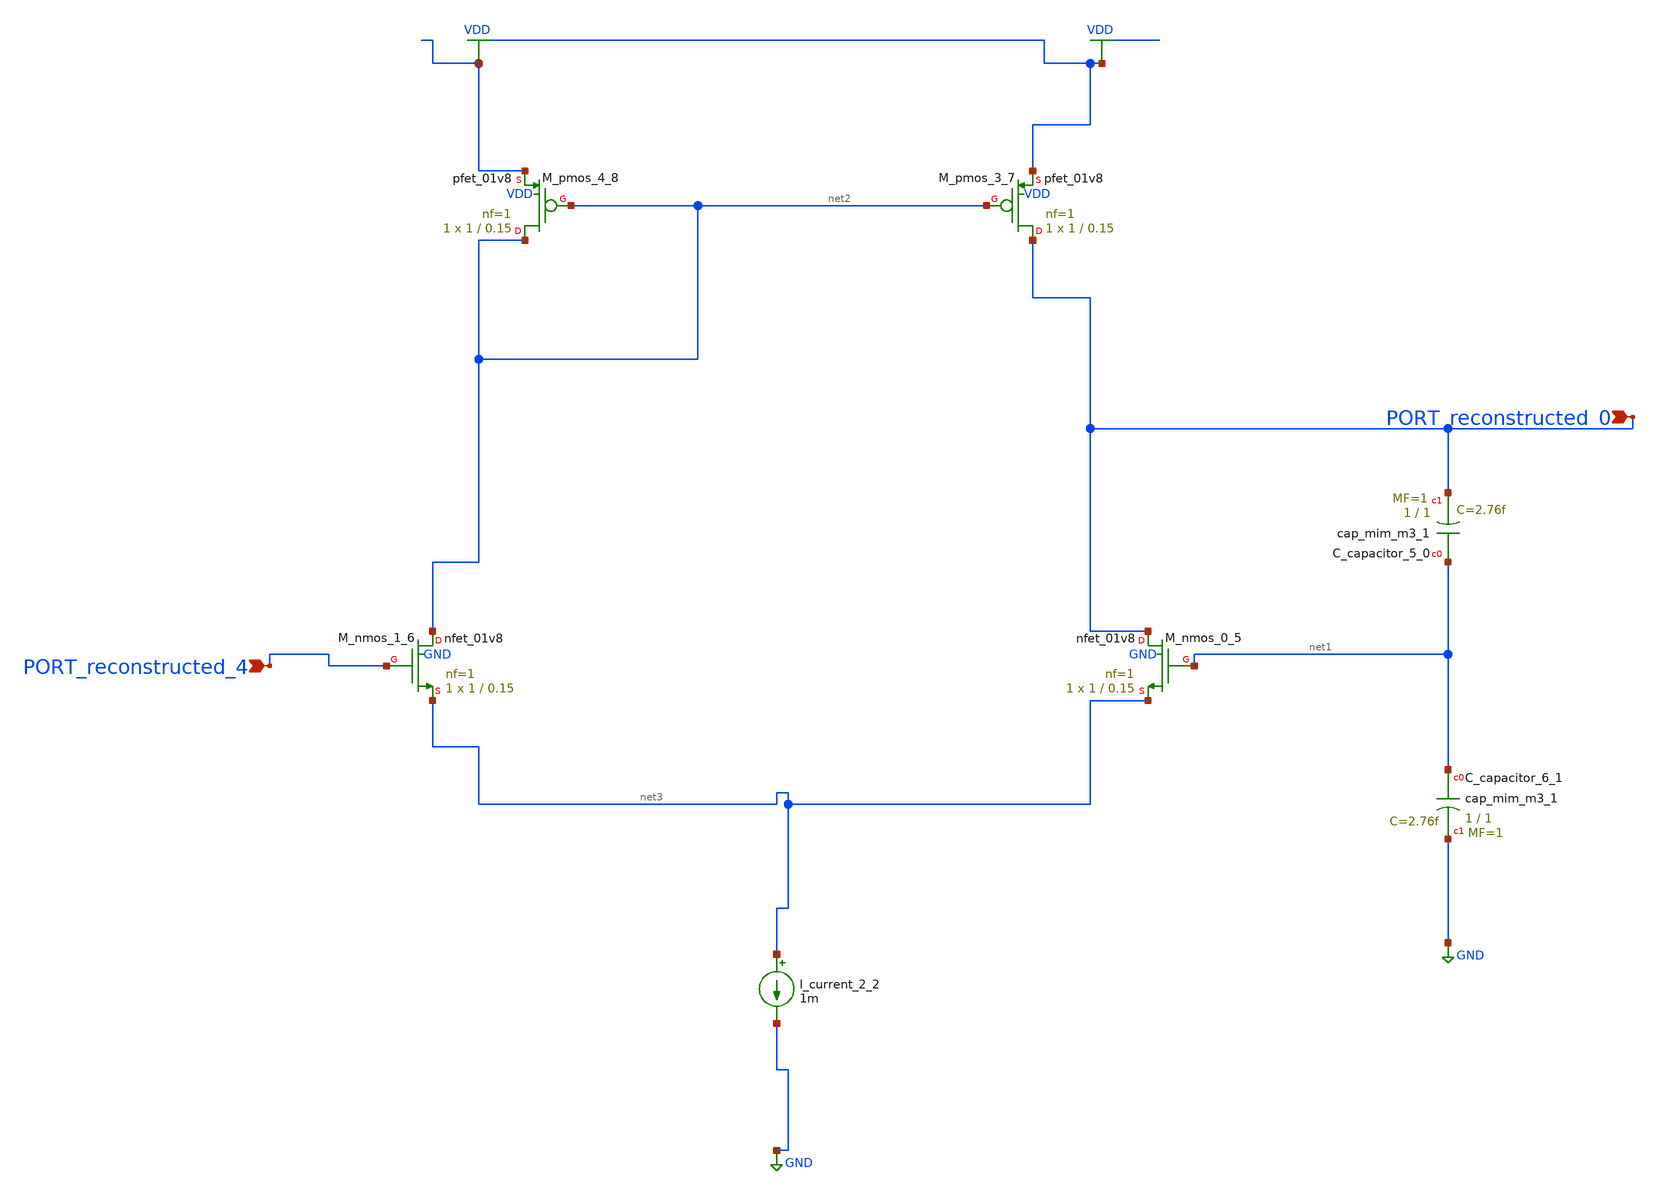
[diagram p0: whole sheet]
** sch_path: schematics/AMSNet/707.sch
**.subckt 707 PORT_reconstructed_0 PORT_reconstructed_4
*.ipin PORT_reconstructed_0
*.ipin PORT_reconstructed_4
XC_capacitor_5_0 net1 PORT_reconstructed_0 sky130_fd_pr__cap_mim_m3_1 W=1 L=1 MF=1 m=1
XC_capacitor_6_1 net1 GND sky130_fd_pr__cap_mim_m3_1 W=1 L=1 MF=1 m=1
I_current_2_2 net3 GND 1m
XM_nmos_0_5 PORT_reconstructed_0 net1 net3 GND sky130_fd_pr__nfet_01v8 L=0.15 W=1 nf=1 ad='int((1 + 1)/2) * 1 / 1 * 0.29'
+ as='int((1 + 2)/2) * 1 / 1 * 0.29' pd='2*int((1 + 1)/2) * (1 / 1 + 0.29)' ps='2*int((1 + 2)/2) * (1 / 1 + 0.29)'
+ nrd='0.29 / 1 ' nrs='0.29 / 1 ' sa=0 sb=0 sd=0 mult=1 m=1
XM_nmos_1_6 net2 PORT_reconstructed_4 net3 GND sky130_fd_pr__nfet_01v8 L=0.15 W=1 nf=1 ad='int((1 + 1)/2) * 1 / 1 * 0.29'
+ as='int((1 + 2)/2) * 1 / 1 * 0.29' pd='2*int((1 + 1)/2) * (1 / 1 + 0.29)' ps='2*int((1 + 2)/2) * (1 / 1 + 0.29)'
+ nrd='0.29 / 1 ' nrs='0.29 / 1 ' sa=0 sb=0 sd=0 mult=1 m=1
XM_pmos_3_7 PORT_reconstructed_0 net2 VDD VDD sky130_fd_pr__pfet_01v8 L=0.15 W=1 nf=1 ad='int((1 + 1)/2) * 1 / 1 * 0.29'
+ as='int((1 + 2)/2) * 1 / 1 * 0.29' pd='2*int((1 + 1)/2) * (1 / 1 + 0.29)' ps='2*int((1 + 2)/2) * (1 / 1 + 0.29)'
+ nrd='0.29 / 1 ' nrs='0.29 / 1 ' sa=0 sb=0 sd=0 mult=1 m=1
XM_pmos_4_8 net2 net2 VDD VDD sky130_fd_pr__pfet_01v8 L=0.15 W=1 nf=1 ad='int((1 + 1)/2) * 1 / 1 * 0.29'
+ as='int((1 + 2)/2) * 1 / 1 * 0.29' pd='2*int((1 + 1)/2) * (1 / 1 + 0.29)' ps='2*int((1 + 2)/2) * (1 / 1 + 0.29)'
+ nrd='0.29 / 1 ' nrs='0.29 / 1 ' sa=0 sb=0 sd=0 mult=1 m=1
**.ends
.GLOBAL GND
.GLOBAL VDD
.end
